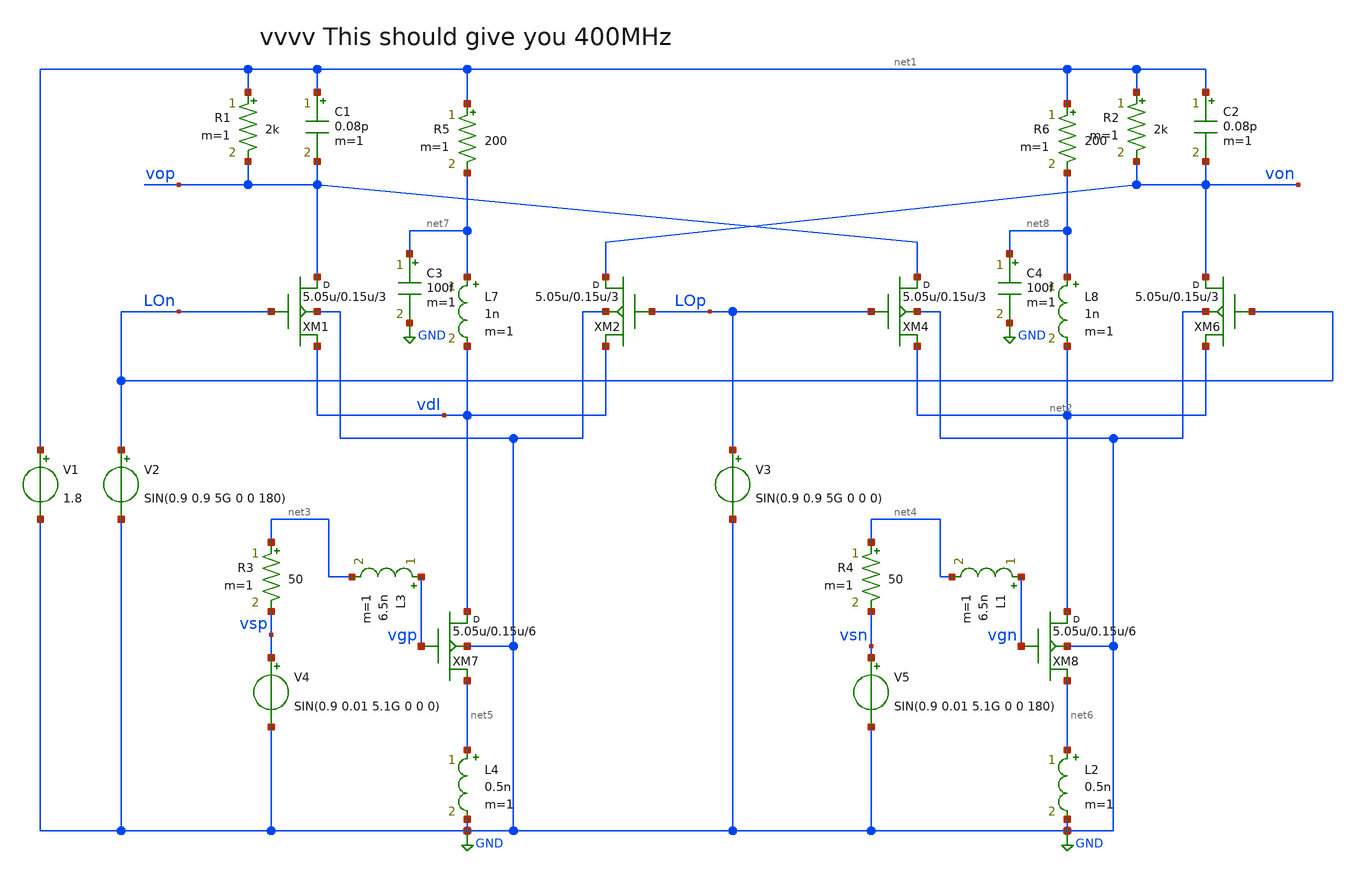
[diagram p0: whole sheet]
** sch_path: xschem/MIXER_5G.sch
**.subckt MIXER_5G
XM1 vop LOn vdl GND sky130_fd_pr__rf_nfet_01v8_bM04W5p00L0p15_ext w=5.05u l=0.15u m=3
XM2 von LOp vdl GND sky130_fd_pr__rf_nfet_01v8_bM04W5p00L0p15_ext w=5.05u l=0.15u m=3
C1 net1 vop 0.08p m=1
R1 net1 vop 2k m=1
C2 net1 von 0.08p m=1
R2 net1 von 2k m=1
V1 net1 GND 1.8
V2 LOn GND SIN(0.9 0.9 5G 0 0 180)
V3 LOp GND SIN(0.9 0.9 5G 0 0 0)
V4 vsp GND SIN(0.9 0.01 5.1G 0 0 0)
XM4 vop LOp net2 GND sky130_fd_pr__rf_nfet_01v8_bM04W5p00L0p15_ext w=5.05u l=0.15u m=3
XM6 von LOn net2 GND sky130_fd_pr__rf_nfet_01v8_bM04W5p00L0p15_ext w=5.05u l=0.15u m=3
V5 vsn GND SIN(0.9 0.01 5.1G 0 0 180)
L3 vgp net3 6.5n m=1
L1 vgn net4 6.5n m=1
L2 net6 GND 0.5n m=1
L4 net5 GND 0.5n m=1
R3 net3 vsp 50 m=1
R4 net4 vsn 50 m=1
XM7 vdl vgp net5 GND sky130_fd_pr__rf_nfet_01v8_bM04W5p00L0p15_ext w=5.05u l=0.15u m=6
XM8 net2 vgn net6 GND sky130_fd_pr__rf_nfet_01v8_bM04W5p00L0p15_ext w=5.05u l=0.15u m=6
L7 net7 vdl 1n m=1
C3 net7 GND 100f m=1
R5 net1 net7 200 m=1
L8 net8 net2 1n m=1
C4 net8 GND 100f m=1
R6 net1 net8 200 m=1
**** begin user architecture code


.subckt sky130_fd_pr__rf_nfet_01v8_bM04W5p00L0p15_ext DRAIN GATE SOURCE SUBSTRATE
X0 DRAIN GATE SOURCE SUBSTRATE sky130_fd_pr__nfet_01v8 ad=2.828e+12p pd=2.132e+07u as=4.242e+12p
+ ps=3.198e+07u w=5.05e+06u l=150000u
X1 SOURCE SUBSTRATE SUBSTRATE SUBSTRATE sky130_fd_pr__nfet_01v8 ad=0p pd=0u as=3.03e+12p
+ ps=2.14e+07u w=5.05e+06u l=150000u
X2 SOURCE GATE DRAIN SUBSTRATE sky130_fd_pr__nfet_01v8 ad=0p pd=0u as=0p ps=0u w=5.05e+06u l=150000u
X3 DRAIN GATE SOURCE SUBSTRATE sky130_fd_pr__nfet_01v8 ad=0p pd=0u as=0p ps=0u w=5.05e+06u l=150000u
X4 SUBSTRATE SUBSTRATE SOURCE SUBSTRATE sky130_fd_pr__nfet_01v8 ad=0p pd=0u as=0p ps=0u w=5.05e+06u
+ l=150000u
X5 SOURCE GATE DRAIN SUBSTRATE sky130_fd_pr__nfet_01v8 ad=0p pd=0u as=0p ps=0u w=5.05e+06u l=150000u
.ends
* .options savecurrents
.tran 0.1ps 20ns
.control
run
display
let vo = v(vop)-v(von)
let vs = v(vsp)-v(vsn)
let vg = v(vgp)-v(vgn)
plot v(von) v(vop)
plot vo
plot vs
plot vg
fft vo vs vg
plot db(vo) db(vs)

.endc


.lib $::SKYWATER_MODELS/sky130.lib.spice tt
* .include $::PDKPATH/libs.ref/sky130_fd_sc_hvl/spice/sky130_fd_sc_hvl.spice

**** end user architecture code
**.ends
.GLOBAL GND
.end
